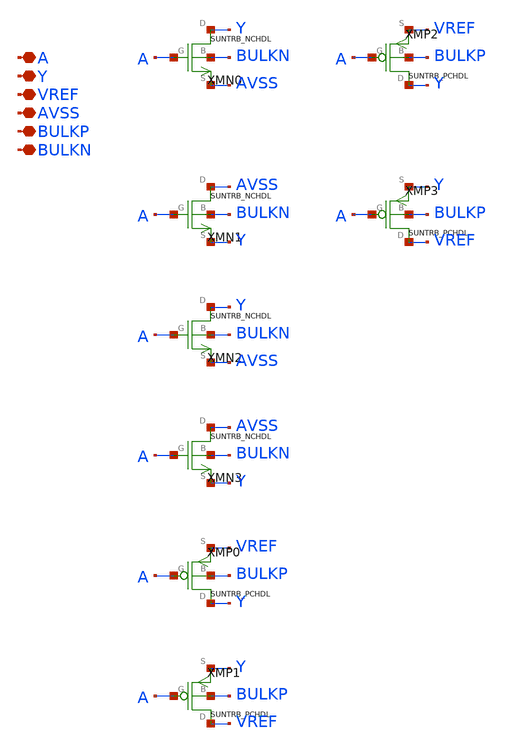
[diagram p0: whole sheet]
** sch_path: ip/sun_trb_sky130nm/design/SUN_TRB_SKY130NM/SUNTRB_SWX4_CV.sch
**.subckt SUNTRB_SWX4_CV A Y VREF AVSS BULKP BULKN
*.iopin A
*.iopin Y
*.iopin VREF
*.iopin AVSS
*.iopin BULKP
*.iopin BULKN
XMN0 Y A AVSS BULKN SUNTRB_NCHDL xoffset=0 yoffset=0 angle=0
XMN1 AVSS A Y BULKN SUNTRB_NCHDL xoffset=0 yoffset=0 angle=0
XMN2 Y A AVSS BULKN SUNTRB_NCHDL xoffset=0 yoffset=0 angle=0
XMN3 AVSS A Y BULKN SUNTRB_NCHDL xoffset=0 yoffset=0 angle=0
XMP0 Y A VREF BULKP SUNTRB_PCHDL xoffset=0 yoffset=0 angle=0
XMP1 VREF A Y BULKP SUNTRB_PCHDL xoffset=0 yoffset=0 angle=0
XMP2 Y A VREF BULKP SUNTRB_PCHDL xoffset=0 yoffset=0 angle=0
XMP3 VREF A Y BULKP SUNTRB_PCHDL xoffset=0 yoffset=0 angle=0
**.ends
.end
